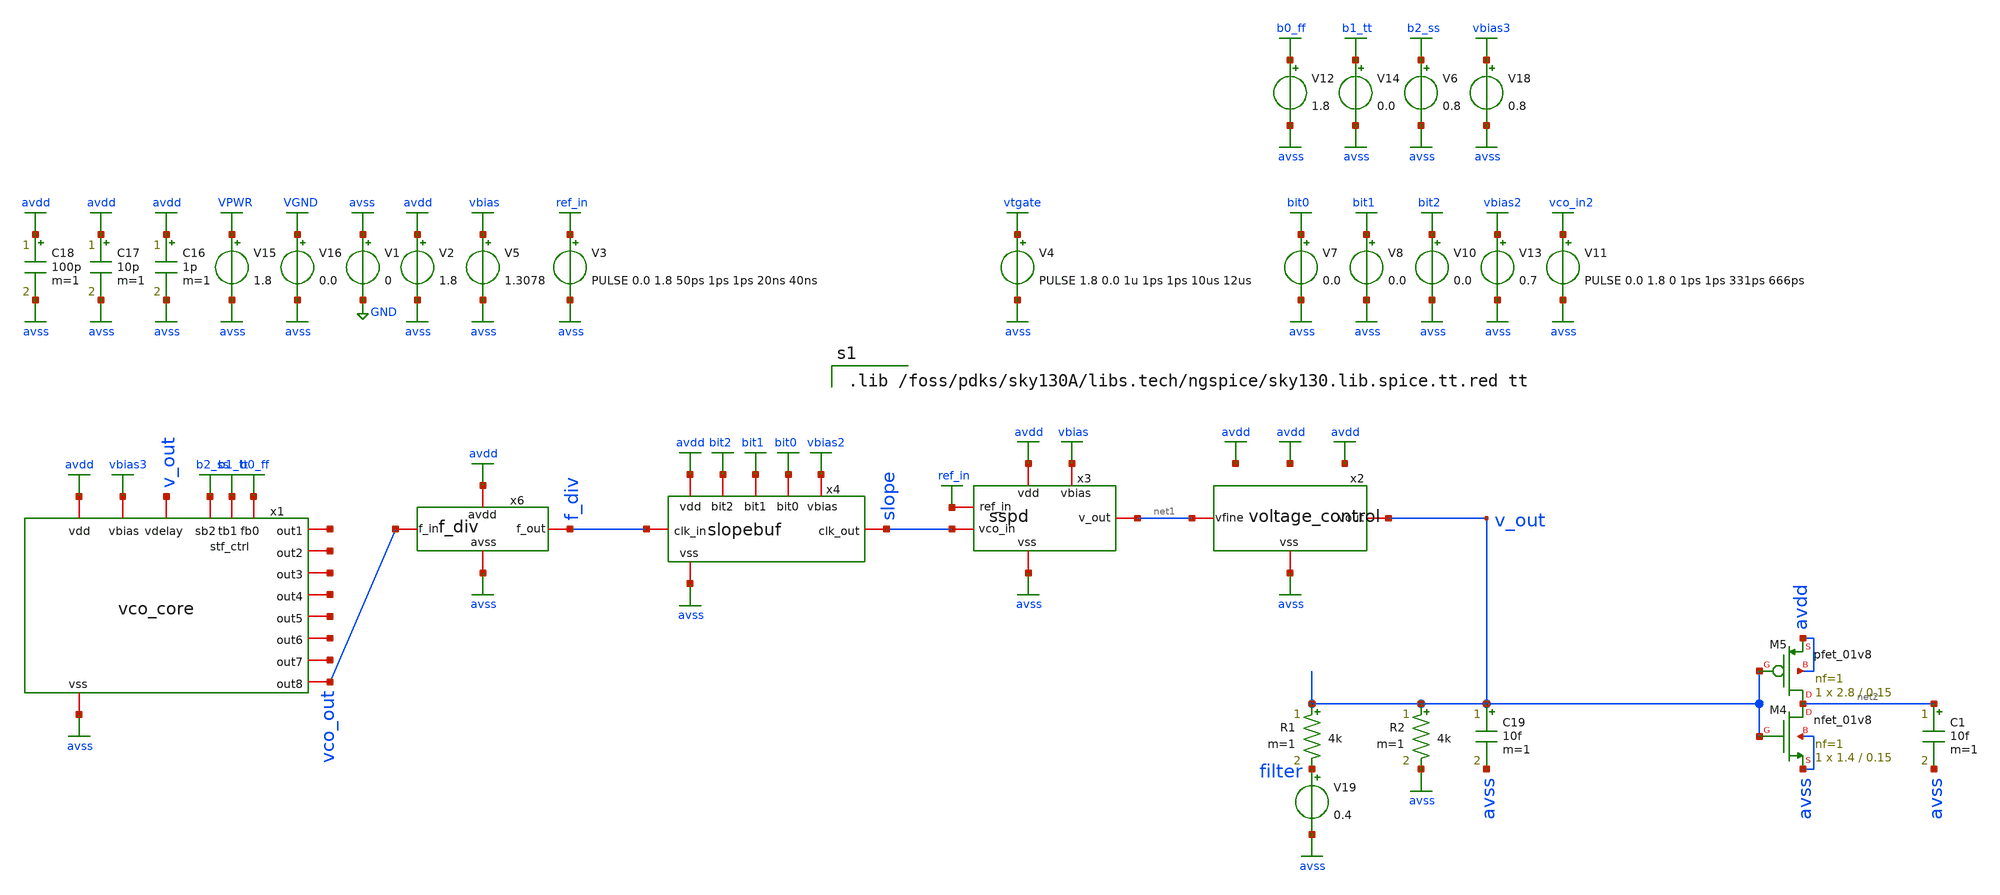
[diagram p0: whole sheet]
** sch_path: xschem/complete_testbench_5.sch
**.subckt complete_testbench_5
V1 avss GND 0
V2 avdd avss 1.8
V3 ref_in avss PULSE 0.0 1.8 50ps 1ps 1ps 20ns 40ns
V5 vbias avss 1.3078
V4 vtgate avss PULSE 1.8 0.0 1u 1ps 1ps 10us 12us
R1 v_out filter 4k m=1
R2 v_out avss 4k m=1
V7 bit0 avss 0.0
V8 bit1 avss 0.0
V10 bit2 avss 0.0
V13 vbias2 avss 0.7
V11 vco_in2 avss PULSE 0.0 1.8 0 1ps 1ps 331ps 666ps
V15 VPWR avss 1.8
V16 VGND avss 0.0
C16 avdd avss 1p m=1
C17 avdd avss 10p m=1
C18 avdd avss 100p m=1
V12 b0_ff avss 1.8
V14 b1_tt avss 0.0
V18 vbias3 avss 0.8
C19 v_out avss 10f m=1
XM4 net2 v_out avss avss sky130_fd_pr__nfet_01v8 L=0.15 W=1.4 nf=1 ad='int((nf+1)/2) * W/nf * 0.29' as='int((nf+2)/2) * W/nf * 0.29'
+ pd='2*int((nf+1)/2) * (W/nf + 0.29)' ps='2*int((nf+2)/2) * (W/nf + 0.29)' nrd='0.29 / W' nrs='0.29 / W'
+ sa=0 sb=0 sd=0 mult=1 m=1
XM5 net2 v_out avdd avdd sky130_fd_pr__pfet_01v8 L=0.15 W=2.8 nf=1 ad='int((nf+1)/2) * W/nf * 0.29' as='int((nf+2)/2) * W/nf * 0.29'
+ pd='2*int((nf+1)/2) * (W/nf + 0.29)' ps='2*int((nf+2)/2) * (W/nf + 0.29)' nrd='0.29 / W' nrs='0.29 / W'
+ sa=0 sb=0 sd=0 mult=1 m=1
V19 filter avss 0.4
x1 avdd net3 avss net4 net5 vbias3 net6 v_out net7 b0_ff b1_tt net8 net9 b2_ss vco_out vco_core
x2 avss net1 v_out voltage_control
x3 avdd avss ref_in slope vbias net1 sspd
x4 avdd avss f_div slope bit0 bit1 bit2 vbias2 slopebuf
x6 avdd avss vco_out f_div f_div
C1 net2 avss 10f m=1
V6 b2_ss avss 0.8
**** begin user architecture code

.lib /foss/pdks/sky130A/libs.tech/ngspice/sky130.lib.spice.tt.red tt



.include /foss/pdks/sky130A/libs.ref/sky130_fd_sc_hd/spice/sky130_fd_sc_hd.spice
.control
save ref_in vco_out f_div slope v_out @V1[i] @V2[i] @V3[i] @V4[i] @V15[i]
tran 0.01n 10000n 10n
run
plot vco_out
plot f_div
plot ref_in slope
plot v_out
plot @V1[i] @V2[i] @V3[i] @V4[i] @V15[i]
fft ref_in vco_out f_div
plot db(mag(ref_in)) db(mag(f_div)) db(mag(vco_out)) xlimit 0.1meg 4g ylimit 5 -60
*compose values values 10.738n 10.666n 10.596n
*foreach val $&values
*	echo run = $val
*	alter @v4[pulse] = [ 1.8 0.0 0 5ps 5ps 5.323ns $val ] $ vector
*	save ref_in vco_in clk nclk v_out @V1[i] @V3[i] s1 s2
*	tran 0.001n 280n 40n
*	run
*end
*plot tran1.vco_in tran2.vco_in tran3.vco_in
*plot tran1.s2 tran2.s2 tran3.s2
*plot tran1.v_out tran2.v_out tran3.v_out
*plot tran1.v_out
*plot tran2.v_out
*plot tran3.v_out
*plot tran1.s2
*plot tran2.s2
*plot tran3.s2
*compose values start=0.0 stop=1.8 step=0.1
*foreach val $&values
*	echo run = $val
*	alter v5 $val
*	save ref_in vco_in clk nclk v_out @V1[i] @V3[i] s1 s2
*	tran 0.05n 280n 40n
*	run
*end
.endc
.end


**** end user architecture code
**.ends
.GLOBAL avdd
.GLOBAL avss
.GLOBAL GND
.GLOBAL ref_in
.GLOBAL vbias
.GLOBAL vtgate
.GLOBAL bit0
.GLOBAL bit1
.GLOBAL bit2
.GLOBAL vbias2
.GLOBAL vco_in2
.GLOBAL VPWR
.GLOBAL VGND
.GLOBAL b0_ff
.GLOBAL b1_tt
.GLOBAL b2_ss
.GLOBAL vbias3
.end
